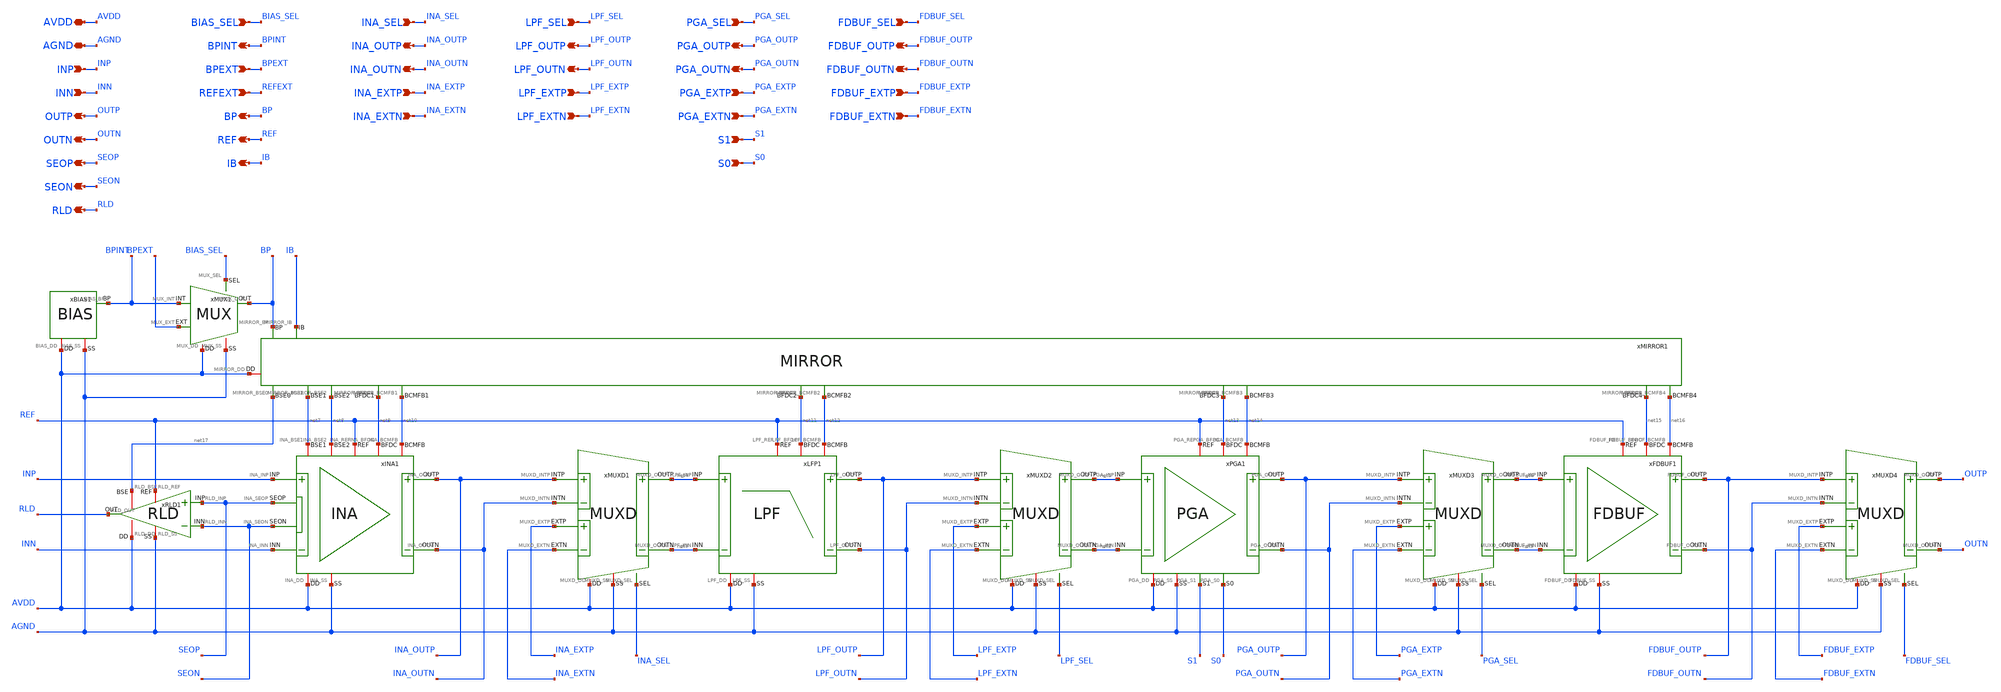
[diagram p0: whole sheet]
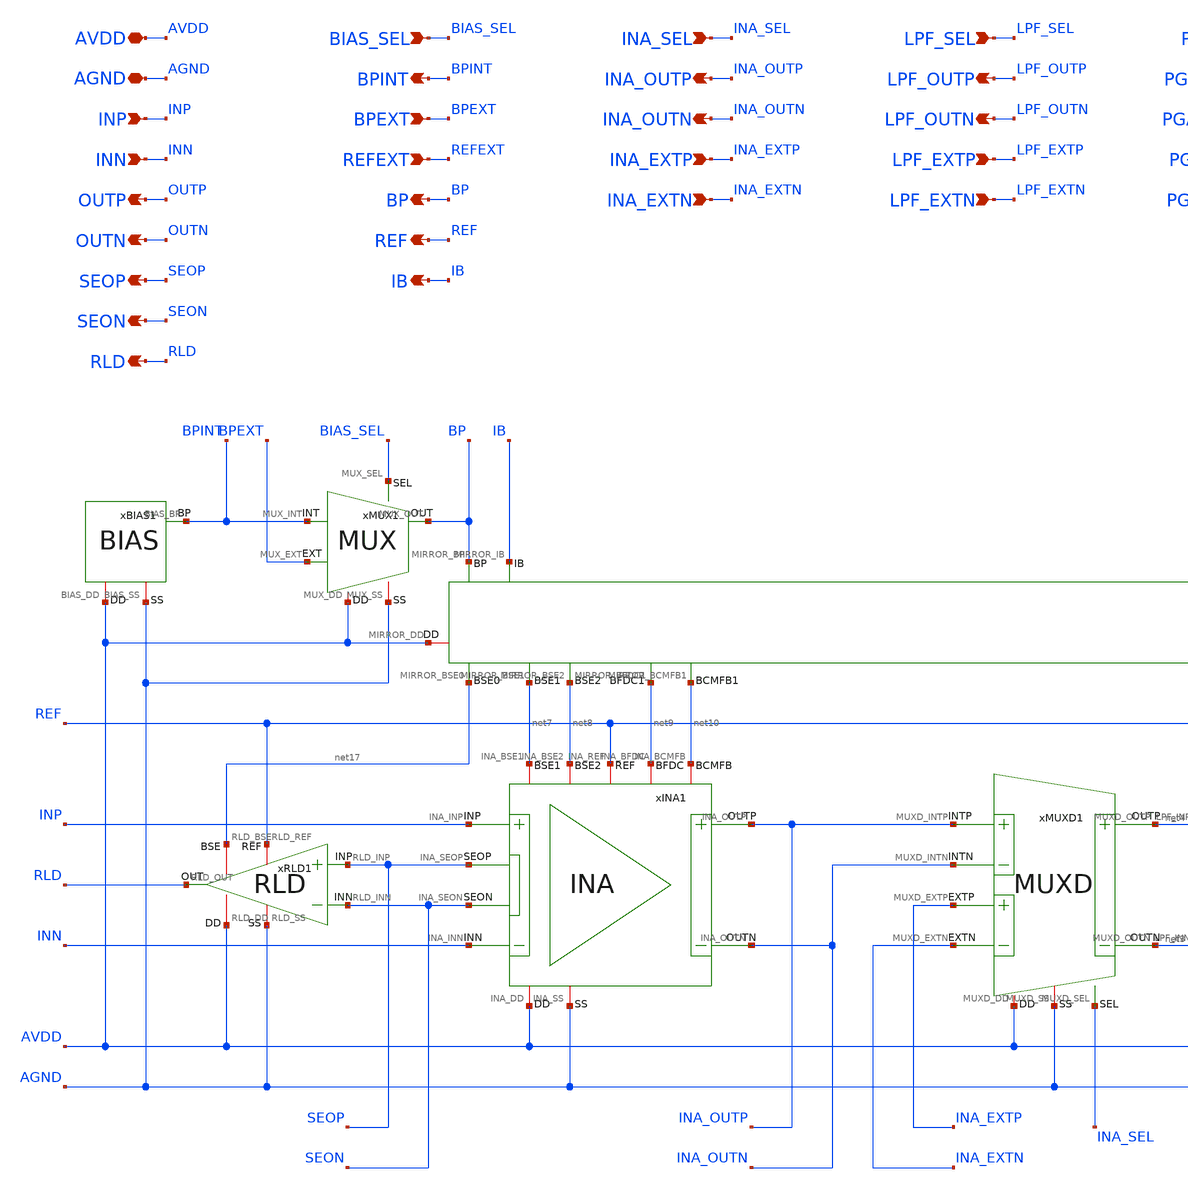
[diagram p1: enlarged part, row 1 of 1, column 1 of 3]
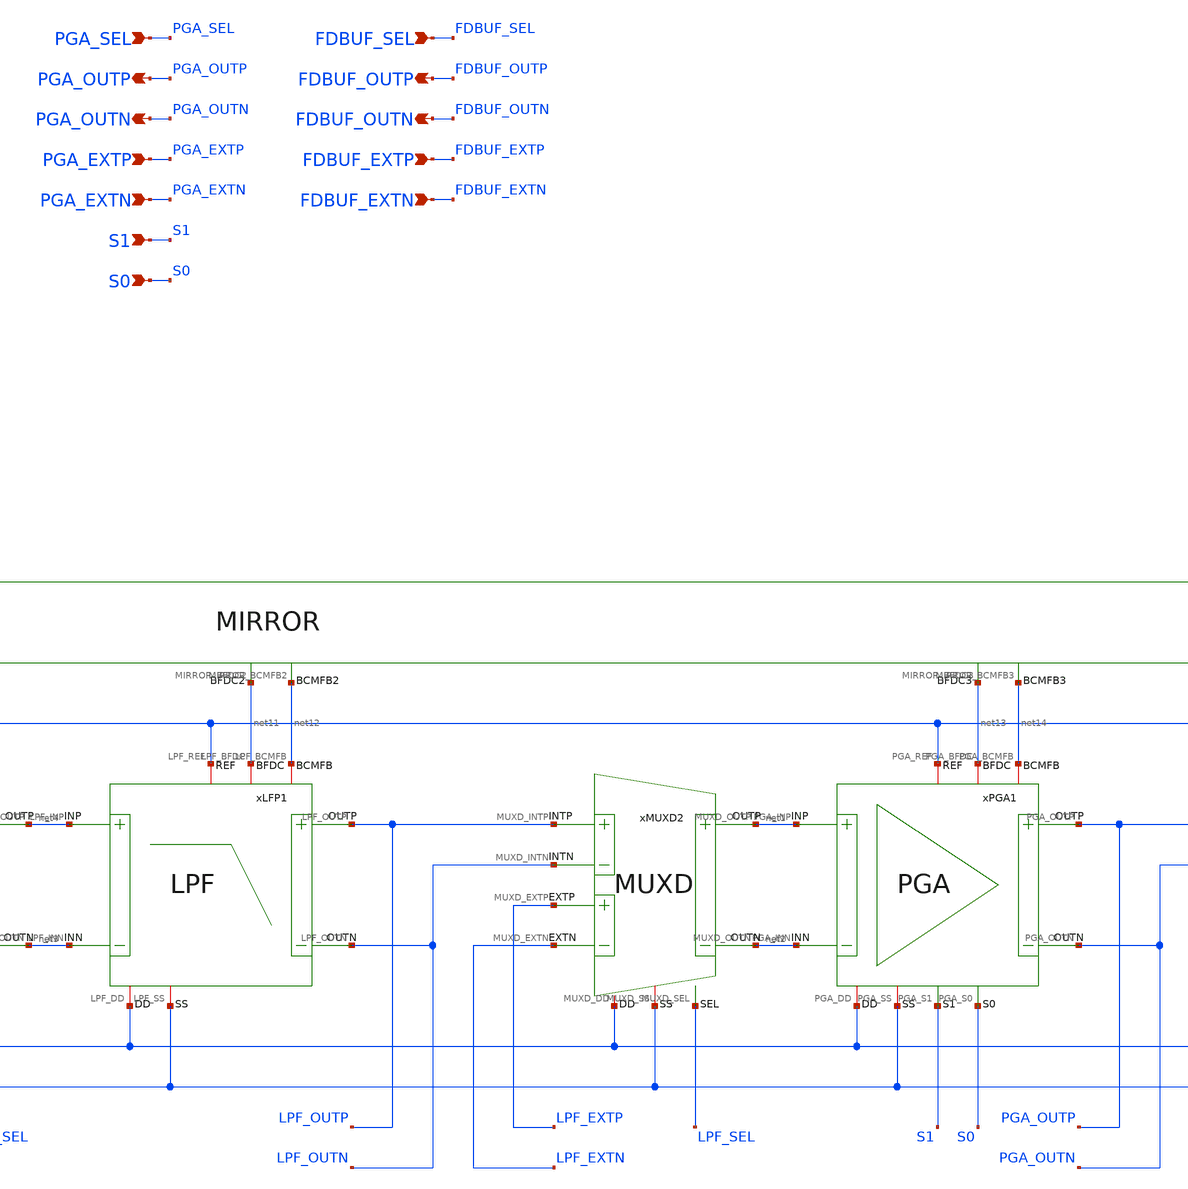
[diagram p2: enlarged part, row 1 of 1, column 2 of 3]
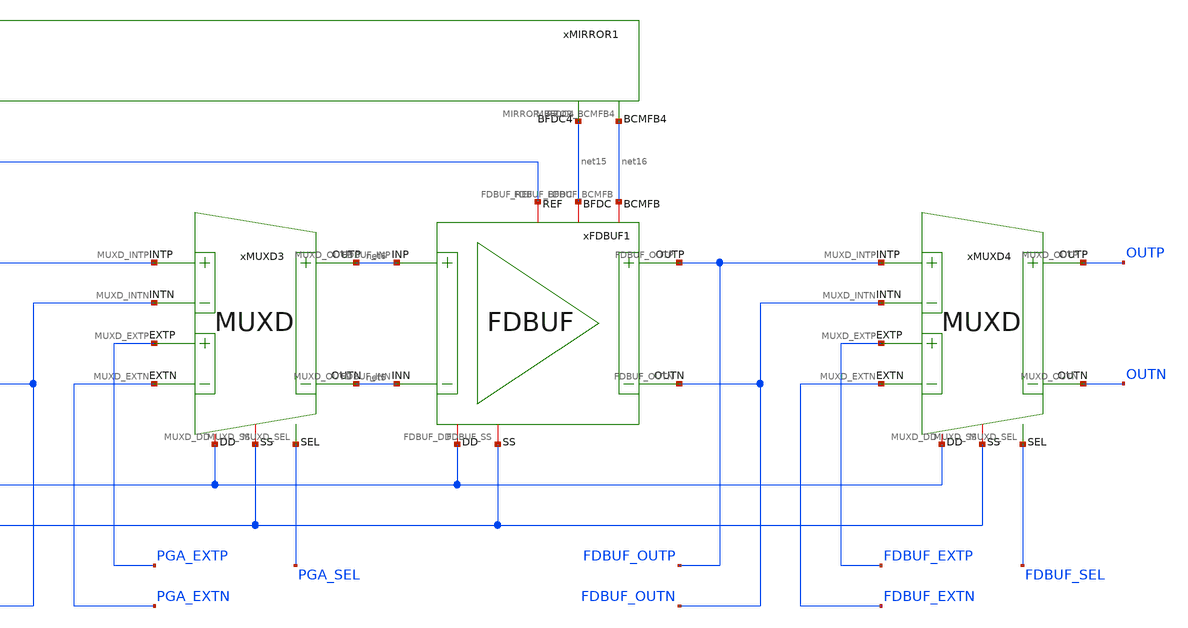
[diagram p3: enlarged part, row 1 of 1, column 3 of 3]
** sch_path: Design_Files/IC Design/Schematic/AFE_BLOCKS/AFE/AFE.sch
**.subckt AFE INA_OUTP INA_OUTN INA_EXTP INA_EXTN LPF_OUTP LPF_OUTN LPF_EXTP LPF_EXTN PGA_OUTP
*+ PGA_OUTN PGA_EXTP PGA_EXTN FDBUF_OUTP FDBUF_OUTN FDBUF_EXTP FDBUF_EXTN AVDD AGND SEOP SEON RLD INP INN BPINT
*+ BPEXT REFEXT BIAS_SEL BP REF INA_SEL LPF_SEL PGA_SEL S1 S0 FDBUF_SEL OUTP OUTN IB
*.opin INA_OUTP
*.opin INA_OUTN
*.ipin INA_EXTP
*.ipin INA_EXTN
*.opin LPF_OUTP
*.opin LPF_OUTN
*.ipin LPF_EXTP
*.ipin LPF_EXTN
*.opin PGA_OUTP
*.opin PGA_OUTN
*.ipin PGA_EXTP
*.ipin PGA_EXTN
*.opin FDBUF_OUTP
*.opin FDBUF_OUTN
*.ipin FDBUF_EXTP
*.ipin FDBUF_EXTN
*.iopin AVDD
*.iopin AGND
*.opin SEOP
*.opin SEON
*.opin RLD
*.ipin INP
*.ipin INN
*.opin BPINT
*.ipin BPEXT
*.ipin REFEXT
*.ipin BIAS_SEL
*.opin BP
*.opin REF
*.ipin INA_SEL
*.ipin LPF_SEL
*.ipin PGA_SEL
*.ipin S1
*.ipin S0
*.ipin FDBUF_SEL
*.opin OUTP
*.opin OUTN
*.opin IB
xLFP1 AVDD AGND net4 net3 LPF_OUTN net11 LPF_OUTP net12 REF LPF
xPGA1 AVDD AGND net1 net2 PGA_OUTN net13 PGA_OUTP net14 REF S1 S0 PGA
xMUXD1 AVDD AGND INA_OUTP INA_OUTN net3 net4 INA_EXTP INA_EXTN INA_SEL MUXD
xINA1 AVDD AGND INP INN INA_OUTN net9 INA_OUTP net10 REF SEON SEOP net7 net8 INA
xMUXD2 AVDD AGND LPF_OUTP LPF_OUTN net2 net1 LPF_EXTP LPF_EXTN LPF_SEL MUXD
xMUXD3 AVDD AGND PGA_OUTP PGA_OUTN net5 net6 PGA_EXTP PGA_EXTN PGA_SEL MUXD
xMUXD4 AVDD AGND FDBUF_OUTP FDBUF_OUTN OUTN OUTP FDBUF_EXTP FDBUF_EXTN FDBUF_SEL MUXD
xRLD1 AVDD AGND SEOP SEON RLD REF net17 RLD
xBIAS1 AVDD AGND BPINT BIAS
xMIRROR1 AVDD BP net17 net7 net8 net9 net11 net13 net15 net10 net12 net14 net16 IB MIRROR
xMUX1 AVDD AGND BPINT BP BPEXT BIAS_SEL MUX
xFDBUF1 AVDD AGND net6 net5 FDBUF_OUTN net15 FDBUF_OUTP net16 REF FDBUF
**.ends
.end
